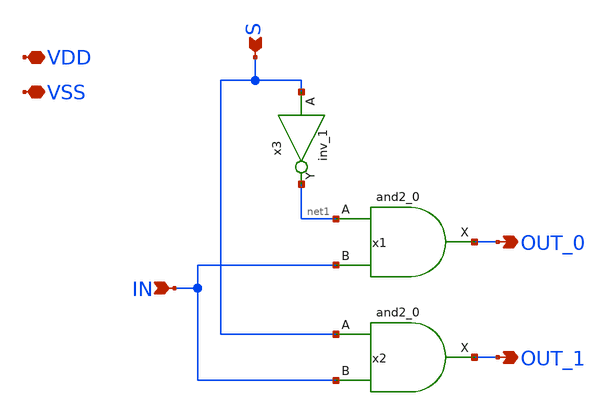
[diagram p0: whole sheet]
** sch_path: xschem/src/demux2/demux2.sch
**.subckt demux2 S OUT_0 IN OUT_1 VDD VSS
*.ipin S
*.opin OUT_0
*.ipin IN
*.opin OUT_1
*.iopin VDD
*.iopin VSS
x1 net1 IN VSS VSS VDD VDD OUT_0 sky130_fd_sc_hd__and2_0
x2 S IN VSS VSS VDD VDD OUT_1 sky130_fd_sc_hd__and2_0
x3 S VSS VSS VDD VDD net1 sky130_fd_sc_hd__inv_1
**** begin user architecture code
 *.include $::SKYWATER_STDCELLS/sky130_fd_sc_hd.spice

**** end user architecture code
**.ends
.end
